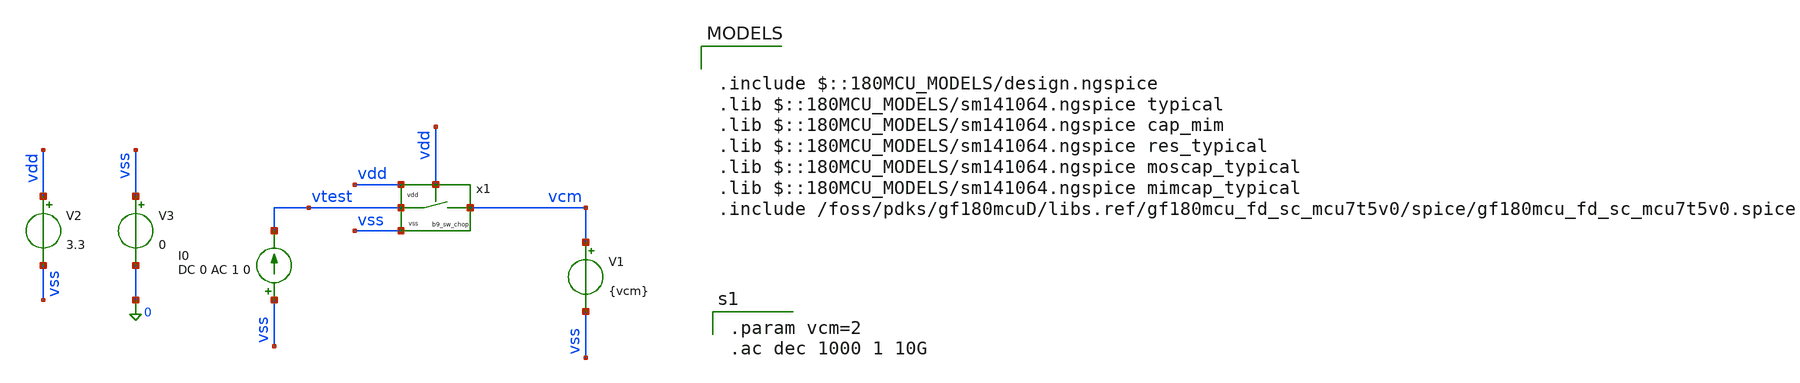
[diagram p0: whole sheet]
** sch_path: xschem/sw/b9_sw_chop_tb_basic.sch
**.subckt b9_sw_chop_tb_basic
x1 vdd vtest vss vcm vdd b9_sw_chop
V1 vcm vss {vcm}
I0 vss vtest DC 0 AC 1 0
V2 vdd vss 3.3
V3 vss 0 0
**** begin user architecture code

.include $::180MCU_MODELS/design.ngspice
.lib $::180MCU_MODELS/sm141064.ngspice typical
.lib $::180MCU_MODELS/sm141064.ngspice cap_mim
.lib $::180MCU_MODELS/sm141064.ngspice res_typical
.lib $::180MCU_MODELS/sm141064.ngspice moscap_typical
.lib $::180MCU_MODELS/sm141064.ngspice mimcap_typical
.include /foss/pdks/gf180mcuD/libs.ref/gf180mcu_fd_sc_mcu7t5v0/spice/gf180mcu_fd_sc_mcu7t5v0.spice


.param vcm=2
.ac dec 1000 1 10G

**** end user architecture code
**.ends

* expanding   symbol:  xschem/sw/b9_sw_chop.sym # of pins=5
** sym_path: xschem/sw/b9_sw_chop.sym
** sch_path: xschem/sw/b9_sw_chop.sch
.subckt b9_sw_chop vdd va vss vb en
*.iopin vdd
*.iopin vss
*.iopin en
*.iopin va
*.iopin vb
XM1 vb en va vss nfet_03v3 L=0.28u W=9.6u nf=4 ad='int((nf+1)/2) * W/nf * 0.18u' as='int((nf+2)/2) * W/nf * 0.18u'
+ pd='2*int((nf+1)/2) * (W/nf + 0.18u)' ps='2*int((nf+2)/2) * (W/nf + 0.18u)' nrd='0.18u / W' nrs='0.18u / W'
+ sa=0 sb=0 sd=0 m=1
.ends

.end
